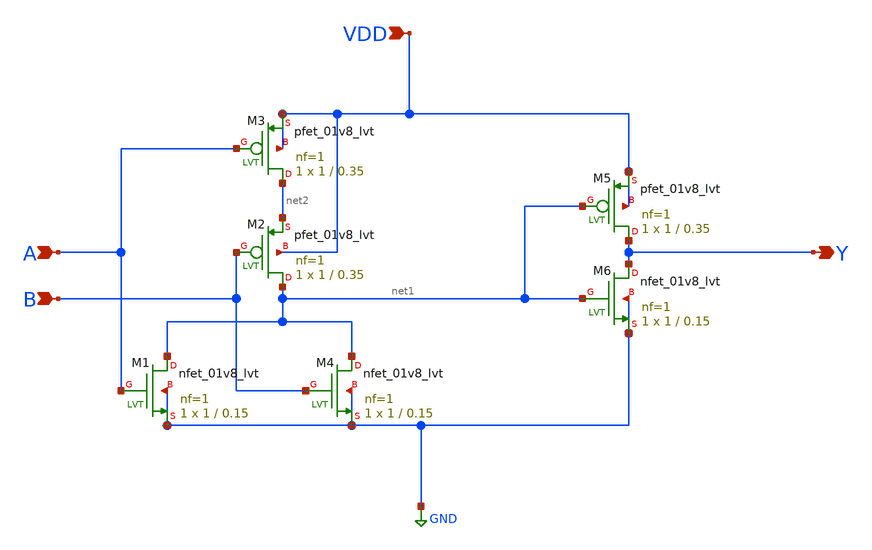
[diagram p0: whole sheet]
** sch_path: Current Sensor/or_new.sch
**.subckt or_new VDD A B Y
*.ipin VDD
*.ipin A
*.ipin B
*.opin Y
XM1 net1 A GND GND sky130_fd_pr__nfet_01v8_lvt L=0.15 W=1 nf=1 ad='int((nf+1)/2) * W/nf * 0.29' as='int((nf+2)/2) * W/nf * 0.29'
+ pd='2*int((nf+1)/2) * (W/nf + 0.29)' ps='2*int((nf+2)/2) * (W/nf + 0.29)' nrd='0.29 / W' nrs='0.29 / W'
+ sa=0 sb=0 sd=0 mult=1 m=1
XM2 net1 B net2 VDD sky130_fd_pr__pfet_01v8_lvt L=0.35 W=1 nf=1 ad='int((nf+1)/2) * W/nf * 0.29' as='int((nf+2)/2) * W/nf * 0.29'
+ pd='2*int((nf+1)/2) * (W/nf + 0.29)' ps='2*int((nf+2)/2) * (W/nf + 0.29)' nrd='0.29 / W' nrs='0.29 / W'
+ sa=0 sb=0 sd=0 mult=1 m=1
XM3 net2 A VDD VDD sky130_fd_pr__pfet_01v8_lvt L=0.35 W=1 nf=1 ad='int((nf+1)/2) * W/nf * 0.29' as='int((nf+2)/2) * W/nf * 0.29'
+ pd='2*int((nf+1)/2) * (W/nf + 0.29)' ps='2*int((nf+2)/2) * (W/nf + 0.29)' nrd='0.29 / W' nrs='0.29 / W'
+ sa=0 sb=0 sd=0 mult=1 m=1
XM4 net1 B GND GND sky130_fd_pr__nfet_01v8_lvt L=0.15 W=1 nf=1 ad='int((nf+1)/2) * W/nf * 0.29' as='int((nf+2)/2) * W/nf * 0.29'
+ pd='2*int((nf+1)/2) * (W/nf + 0.29)' ps='2*int((nf+2)/2) * (W/nf + 0.29)' nrd='0.29 / W' nrs='0.29 / W'
+ sa=0 sb=0 sd=0 mult=1 m=1
XM5 Y net1 VDD VDD sky130_fd_pr__pfet_01v8_lvt L=0.35 W=1 nf=1 ad='int((nf+1)/2) * W/nf * 0.29' as='int((nf+2)/2) * W/nf * 0.29'
+ pd='2*int((nf+1)/2) * (W/nf + 0.29)' ps='2*int((nf+2)/2) * (W/nf + 0.29)' nrd='0.29 / W' nrs='0.29 / W'
+ sa=0 sb=0 sd=0 mult=1 m=1
XM6 Y net1 GND GND sky130_fd_pr__nfet_01v8_lvt L=0.15 W=1 nf=1 ad='int((nf+1)/2) * W/nf * 0.29' as='int((nf+2)/2) * W/nf * 0.29'
+ pd='2*int((nf+1)/2) * (W/nf + 0.29)' ps='2*int((nf+2)/2) * (W/nf + 0.29)' nrd='0.29 / W' nrs='0.29 / W'
+ sa=0 sb=0 sd=0 mult=1 m=1
**.ends
.GLOBAL GND
.end
